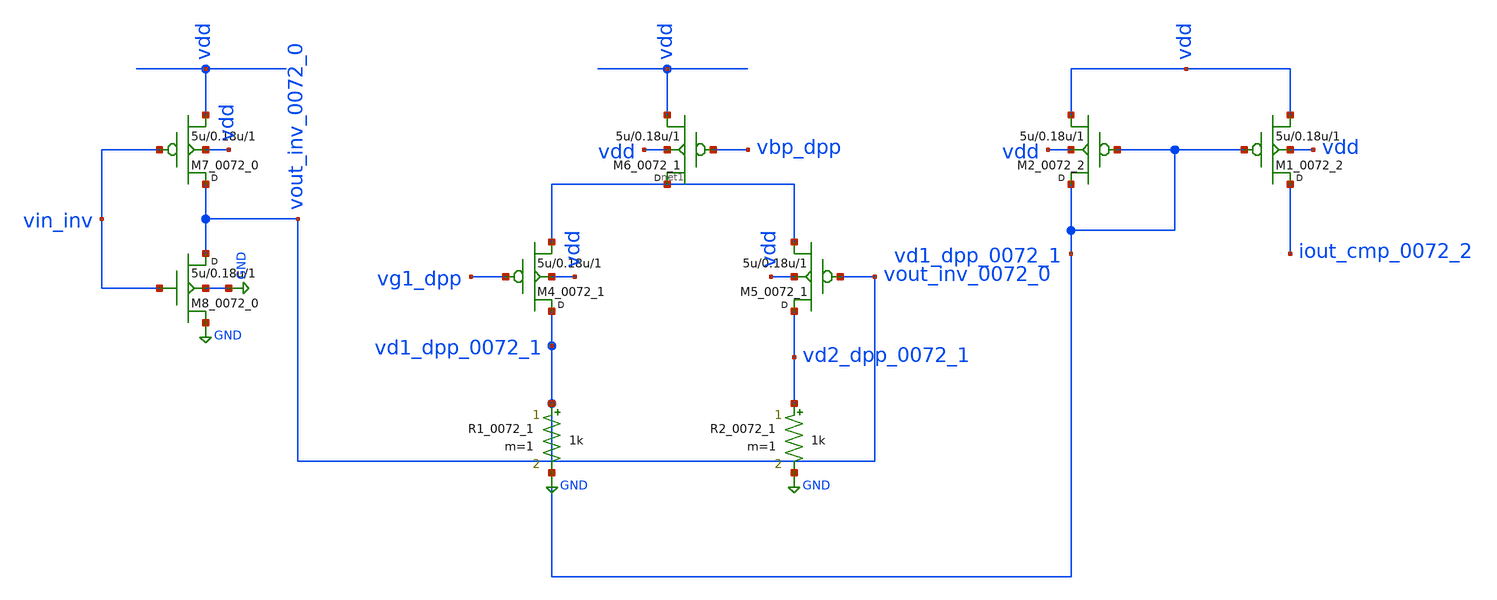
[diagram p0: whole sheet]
** sch_path: synthetic/generated/0072_generated.sch
**.subckt 0072_generated
M7_0072_0 vout_inv_0072_0 vin_inv vdd vdd pmos w=5u l=0.18u m=1
M8_0072_0 vout_inv_0072_0 vin_inv GND GND nmos w=5u l=0.18u m=1
M4_0072_1 vd1_dpp_0072_1 vg1_dpp net1 vdd pmos w=5u l=0.18u m=1
M5_0072_1 vd2_dpp_0072_1 vout_inv_0072_0 net1 vdd pmos w=5u l=0.18u m=1
M6_0072_1 net1 vbp_dpp vdd vdd pmos w=5u l=0.18u m=1
R1_0072_1 vd1_dpp_0072_1 vd1_dpp_0072_1 1k m=1
R2_0072_1 vd2_dpp_0072_1 GND 1k m=1
M1_0072_2 iout_cmp_0072_2 vd1_dpp_0072_1 vdd vdd pmos w=5u l=0.18u m=1
M2_0072_2 vd1_dpp_0072_1 vd1_dpp_0072_1 vdd vdd pmos w=5u l=0.18u m=1
**.ends
.GLOBAL GND
.end
